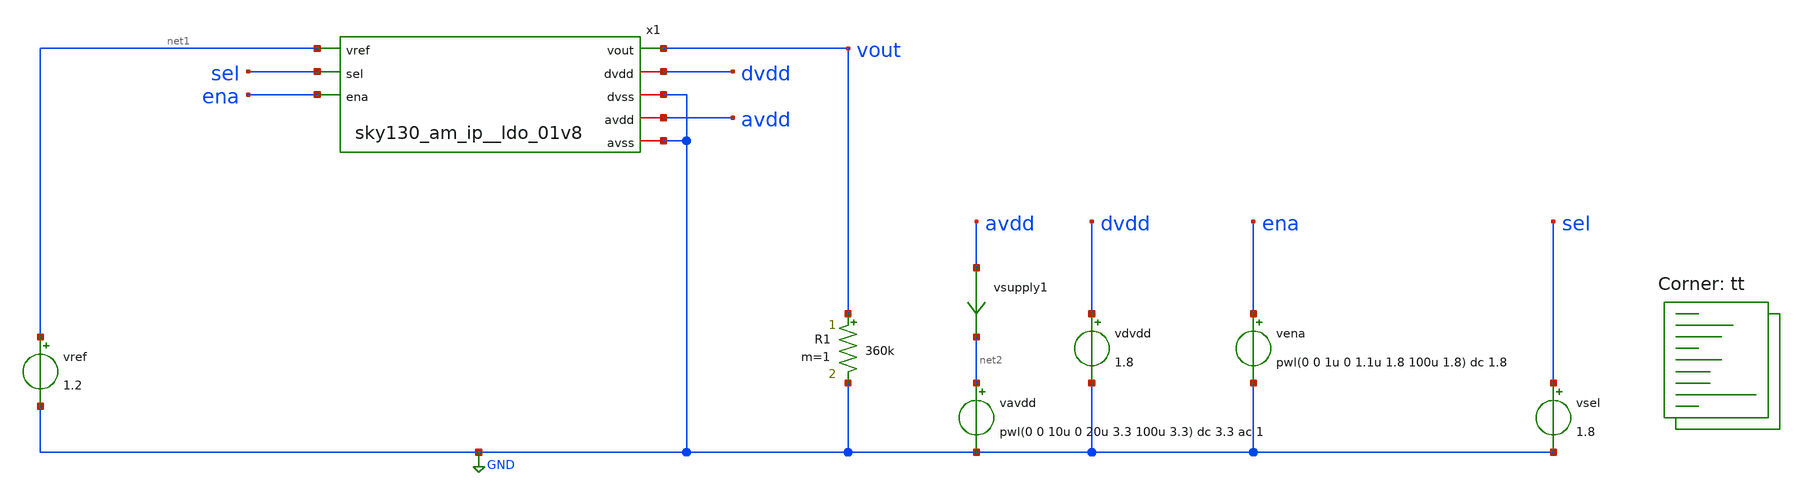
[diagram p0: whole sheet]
** sch_path: xschem/sky130_am_ip__ldo_01v8_tb.sch
**.subckt sky130_am_ip__ldo_01v8_tb
x1 net1 vout sel ena dvdd GND avdd GND sky130_am_ip__ldo_01v8
R1 vout GND 360k m=1
vavdd net2 GND pwl(0 0 10u 0 20u 3.3 100u 3.3) dc 3.3 ac 1
vsupply1 avdd net2 0
.save i(vsupply1)
vena ena GND pwl(0 0 1u 0 1.1u 1.8 100u 1.8) dc 1.8
vdvdd dvdd GND 1.8
vref net1 GND 1.2
vsel sel GND 1.8
**** begin user architecture code

.option savecurrents
.control
save all

op
write sky130_am_ip__ldo_01v8_tb.raw
set appendwrite

ac dec 10 10 1e9
set units=degrees
plot db(vout)

dc vavdd 0 3.3 10m
plot vout

tran 100n 100u
plot vout ena avdd x1.ref_int
.endc


.lib $::SKYWATER_MODELS/sky130.lib.spice tt
**** end user architecture code
**.ends
.GLOBAL GND
.end
